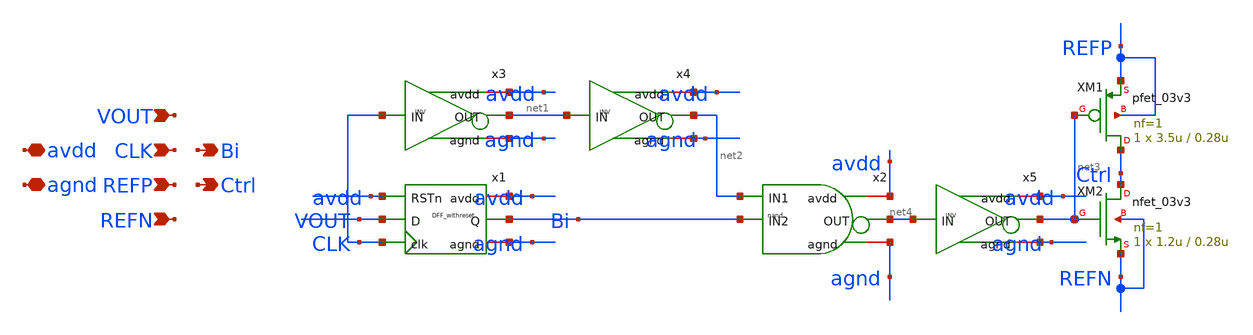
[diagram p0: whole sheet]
** sch_path: mpw18h1/cisar-gen/xschem/TBD/SAR_DAC.sch
**.subckt SAR_DAC agnd Ctrl CLK REFP Bi avdd REFN VOUT
*.iopin agnd
*.opin Ctrl
*.ipin CLK
*.ipin REFP
*.opin Bi
*.iopin avdd
*.ipin REFN
*.ipin VOUT
x1 avdd avdd Bi VOUT CLK agnd DFF_withreset
x2 avdd net2 net4 Bi agnd nand
x3 avdd net1 CLK agnd INV
x4 avdd net2 net1 agnd INV
XM1 Ctrl net3 REFP REFP pfet_03v3 L=0.28u W=3.5u nf=1 ad='int((nf+1)/2) * W/nf * 0.18u' as='int((nf+2)/2) * W/nf * 0.18u'
+ pd='2*int((nf+1)/2) * (W/nf + 0.18u)' ps='2*int((nf+2)/2) * (W/nf + 0.18u)' nrd='0.18u / W' nrs='0.18u / W'
+ sa=0 sb=0 sd=0 m=1
XM2 Ctrl net3 REFN REFN nfet_03v3 L=0.28u W=1.2u nf=1 ad='int((nf+1)/2) * W/nf * 0.18u' as='int((nf+2)/2) * W/nf * 0.18u'
+ pd='2*int((nf+1)/2) * (W/nf + 0.18u)' ps='2*int((nf+2)/2) * (W/nf + 0.18u)' nrd='0.18u / W' nrs='0.18u / W'
+ sa=0 sb=0 sd=0 m=1
x5 avdd net3 net4 agnd INV
**.ends
.end
